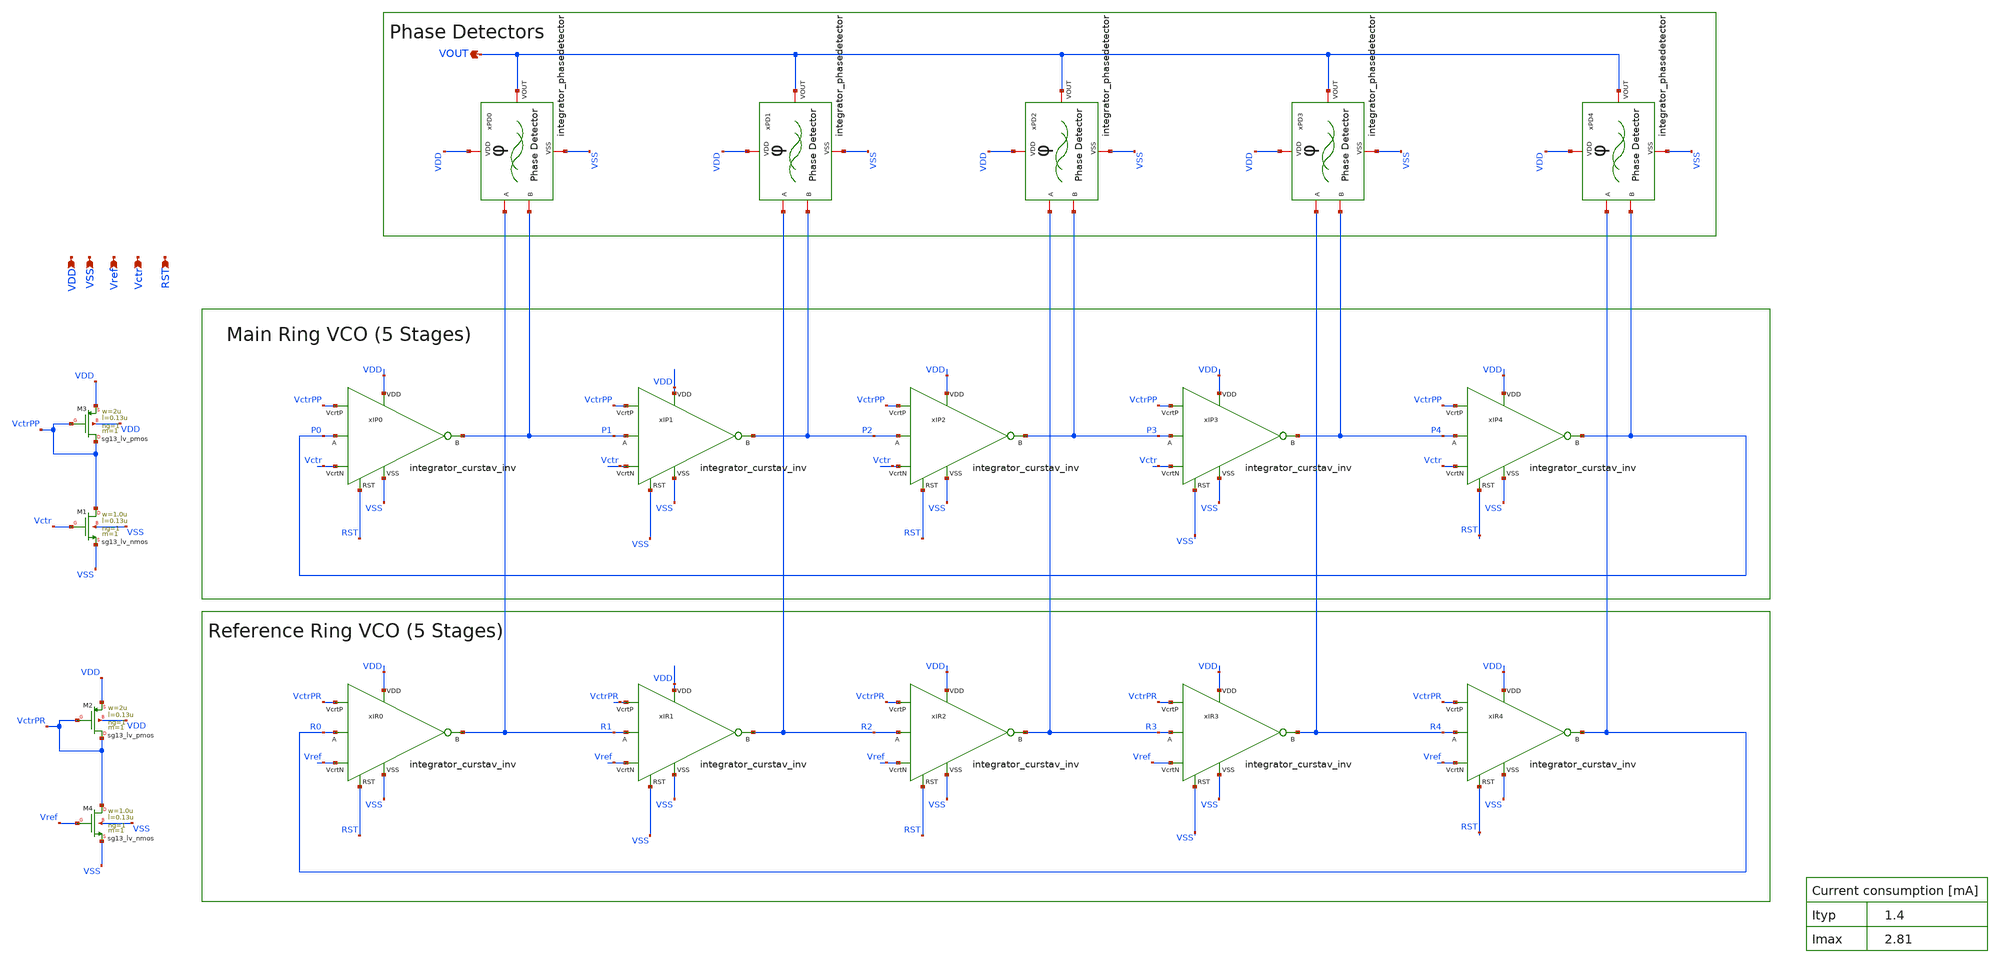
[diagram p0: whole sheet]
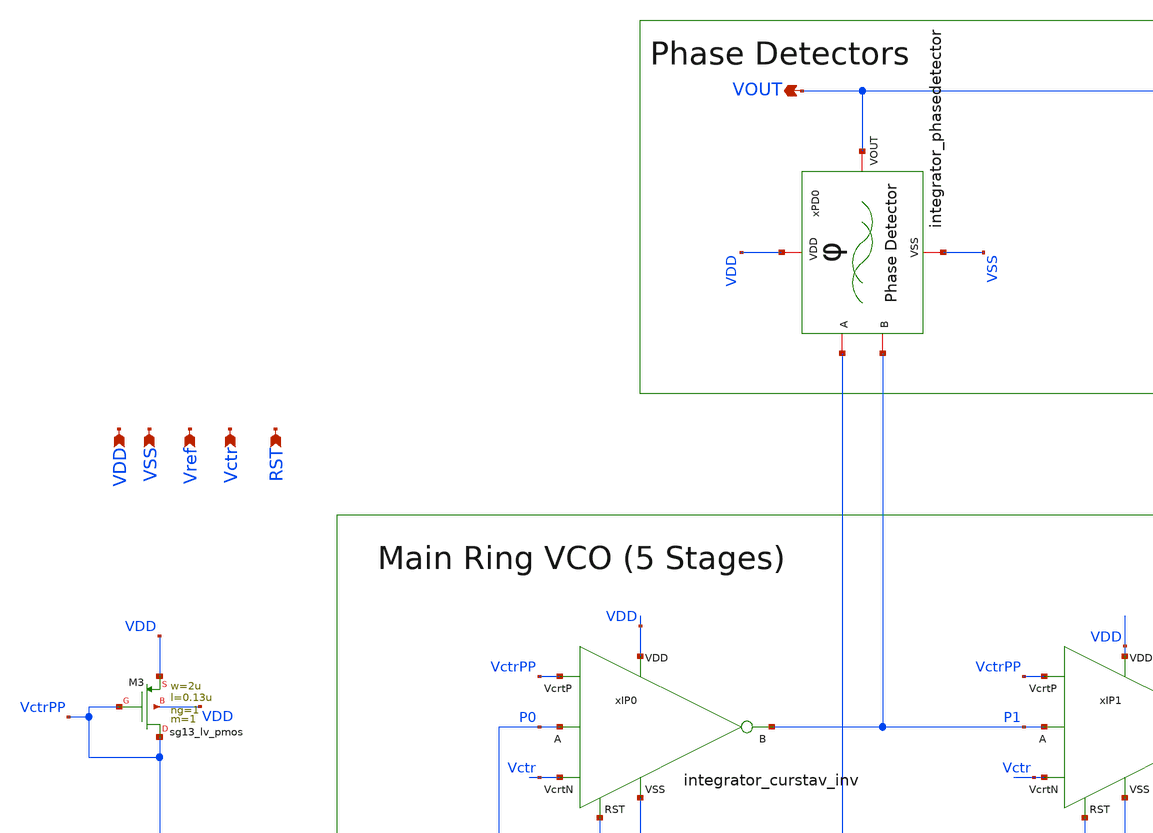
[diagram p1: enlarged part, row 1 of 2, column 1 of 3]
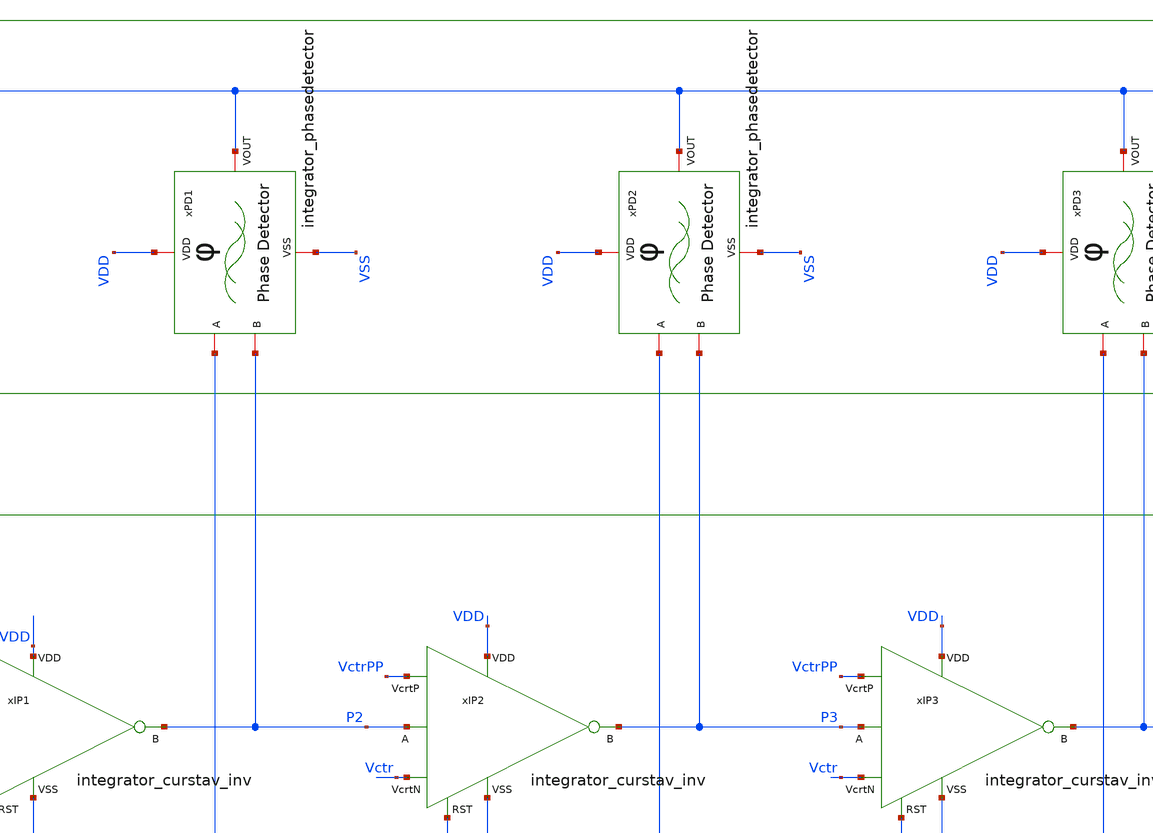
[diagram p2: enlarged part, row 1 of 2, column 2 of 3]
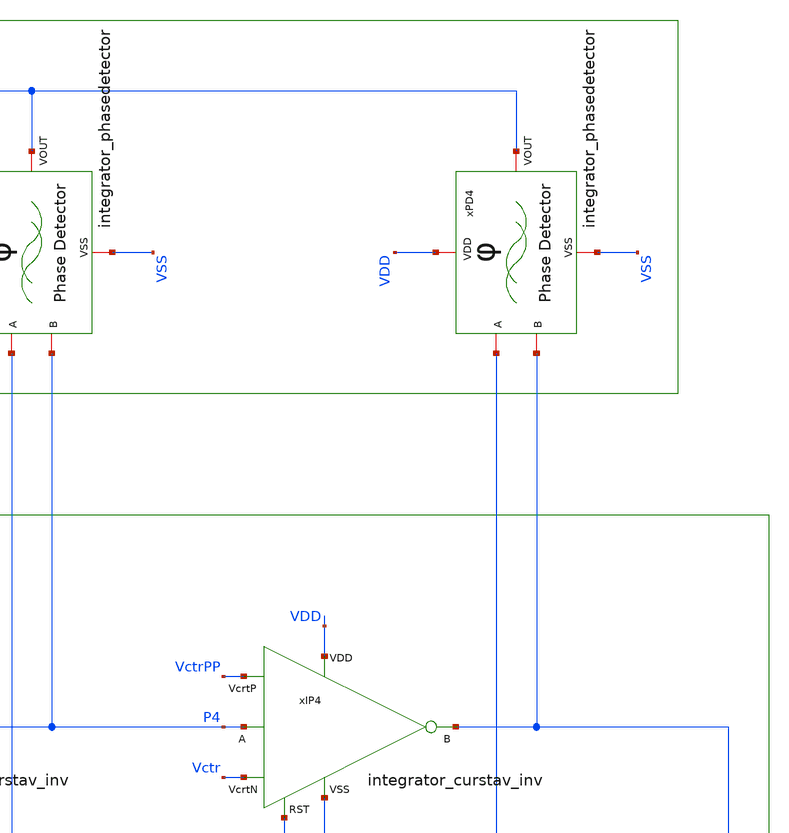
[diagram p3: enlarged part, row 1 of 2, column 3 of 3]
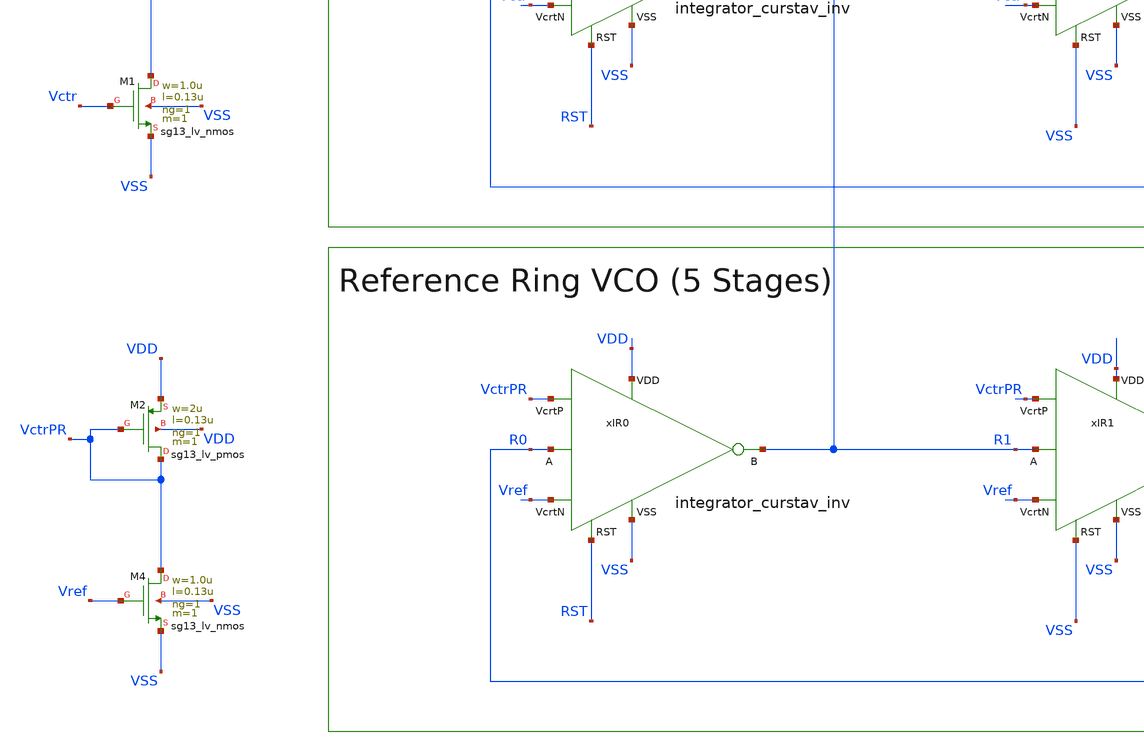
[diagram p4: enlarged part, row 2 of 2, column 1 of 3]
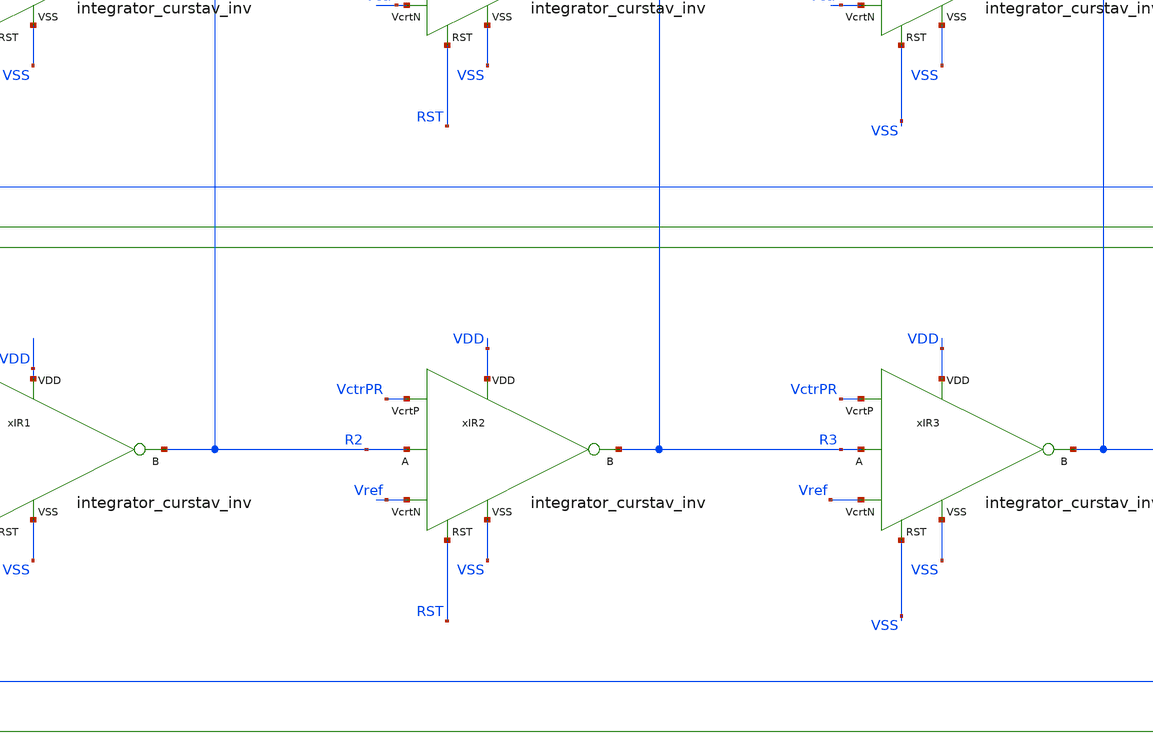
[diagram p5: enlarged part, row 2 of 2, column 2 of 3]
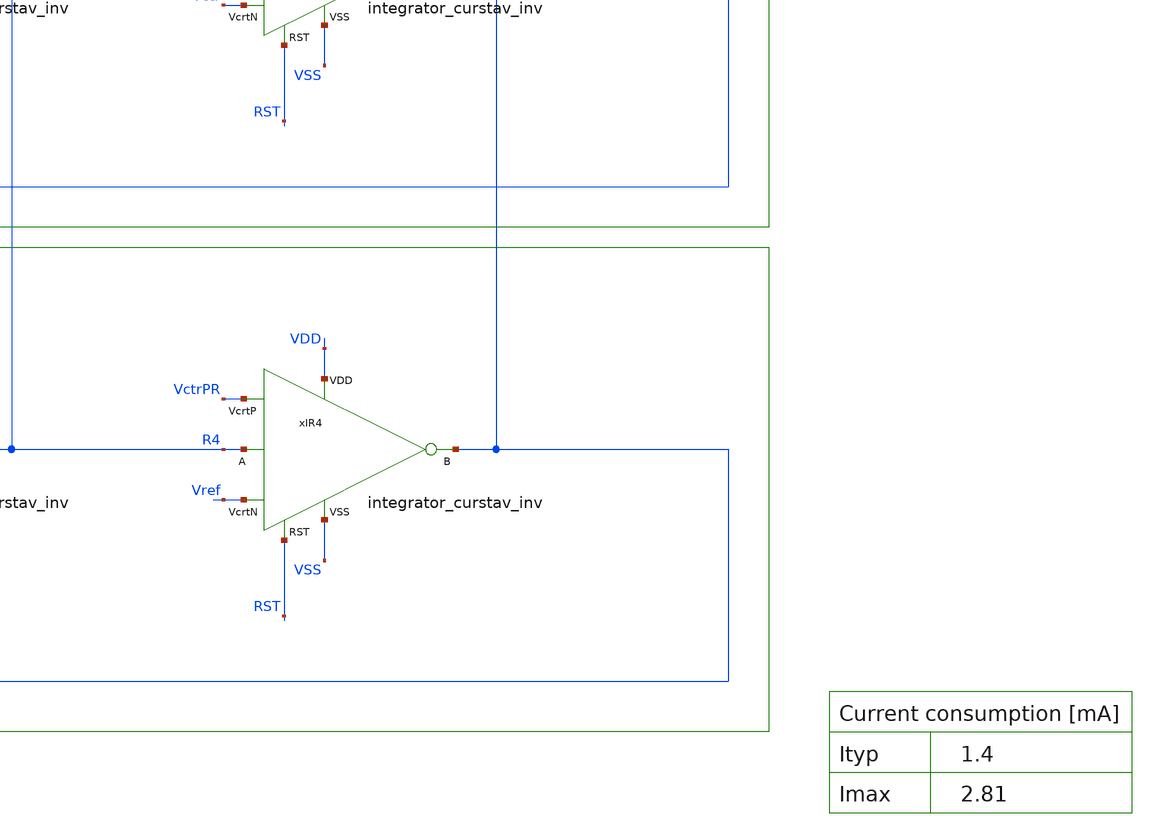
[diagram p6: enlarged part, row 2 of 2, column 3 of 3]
** sch_path: OSC9996-main/schematic/xschem/integrator.sch
**.subckt integrator VSS Vref Vctr VDD RST VOUT
*.ipin VSS
*.ipin Vref
*.ipin Vctr
*.ipin VDD
*.ipin RST
*.opin VOUT
xIP0 VDD VctrPP P0 P1 Vctr VSS RST integrator_curstav_inv
xIP1 VDD VctrPP P1 P2 Vctr VSS VSS integrator_curstav_inv
xIP2 VDD VctrPP P2 P3 Vctr VSS RST integrator_curstav_inv
xIP3 VDD VctrPP P3 P4 Vctr VSS VSS integrator_curstav_inv
xIP4 VDD VctrPP P4 P0 Vctr VSS RST integrator_curstav_inv
xPD0 VDD R1 VOUT P1 VSS integrator_phasedetector
xPD1 VDD R2 VOUT P2 VSS integrator_phasedetector
xPD2 VDD R3 VOUT P3 VSS integrator_phasedetector
xPD3 VDD R4 VOUT P4 VSS integrator_phasedetector
xPD4 VDD R0 VOUT P0 VSS integrator_phasedetector
XM1 VctrPP Vctr VSS VSS sg13_lv_nmos w=1.0u l=0.13u ng=1 m=1 mm_ok=1
XM3 VctrPP VctrPP VDD VDD sg13_lv_pmos w=2u l=0.13u ng=1 m=1 mm_ok=1
XM2 VctrPR VctrPR VDD VDD sg13_lv_pmos w=2u l=0.13u ng=1 m=1 mm_ok=1
XM4 VctrPR Vref VSS VSS sg13_lv_nmos w=1.0u l=0.13u ng=1 m=1 mm_ok=1
xIR0 VDD VctrPR R0 R1 Vref VSS RST integrator_curstav_inv
xIR1 VDD VctrPR R1 R2 Vref VSS VSS integrator_curstav_inv
xIR2 VDD VctrPR R2 R3 Vref VSS RST integrator_curstav_inv
xIR3 VDD VctrPR R3 R4 Vref VSS VSS integrator_curstav_inv
xIR4 VDD VctrPR R4 R0 Vref VSS RST integrator_curstav_inv
**.ends
.end
